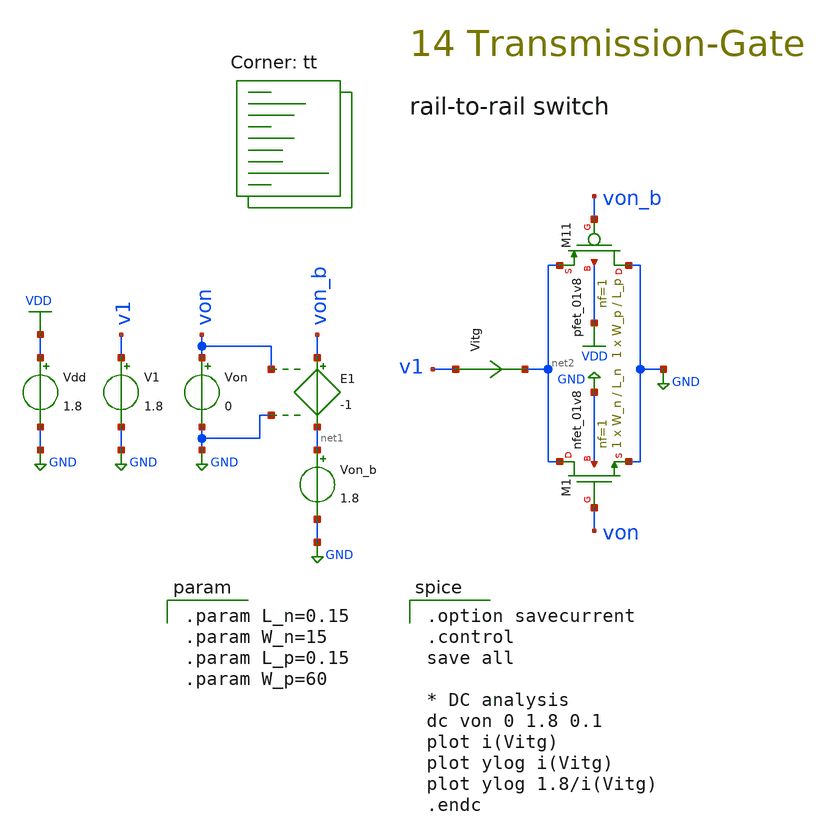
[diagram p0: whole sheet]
** sch_path: 14-a_transmission-gate.sch
**.subckt 14-a_transmission-gate
XM1 net2 von GND GND sky130_fd_pr__nfet_01v8 L=L_n W=W_n nf=1 ad='int((1 + 1)/2) * W_n / 1 * 0.29' as='int((1 + 2)/2) * W_n / 1 * 0.29'
+ pd='2*int((1 + 1)/2) * (W_n / 1 + 0.29)' ps='2*int((1 + 2)/2) * (W_n / 1 + 0.29)' nrd='0.29 / W_n ' nrs='0.29 / W_n '
+ sa=0 sb=0 sd=0 mult=1 m=1
V1 v1 GND 1.8
Von von GND 0
E1 von_b net1 von GND -1
Von_b net1 GND 1.8
XM11 GND von_b net2 VDD sky130_fd_pr__pfet_01v8 L=L_p W=W_p nf=1 ad='int((nf+1)/2) * W/nf * 0.29' as='int((nf+2)/2) * W/nf * 0.29'
+ pd='2*int((nf+1)/2) * (W/nf + 0.29)' ps='2*int((nf+2)/2) * (W/nf + 0.29)' nrd='0.29 / W' nrs='0.29 / W'
+ sa=0 sb=0 sd=0 mult=1 m=1
Vdd VDD GND 1.8
Vitg v1 net2 0
.save i(vitg)
**** begin user architecture code
.lib $::SKYWATER_MODELS/sky130.lib.spice tt

.option savecurrent
.control
save all

* DC analysis
dc von 0 1.8 0.1
plot i(Vitg)
plot ylog i(Vitg)
plot ylog 1.8/i(Vitg)
.endc


.param L_n=0.15
.param W_n=15
.param L_p=0.15
.param W_p=60

**** end user architecture code
**.ends
.GLOBAL GND
.GLOBAL VDD
.end
